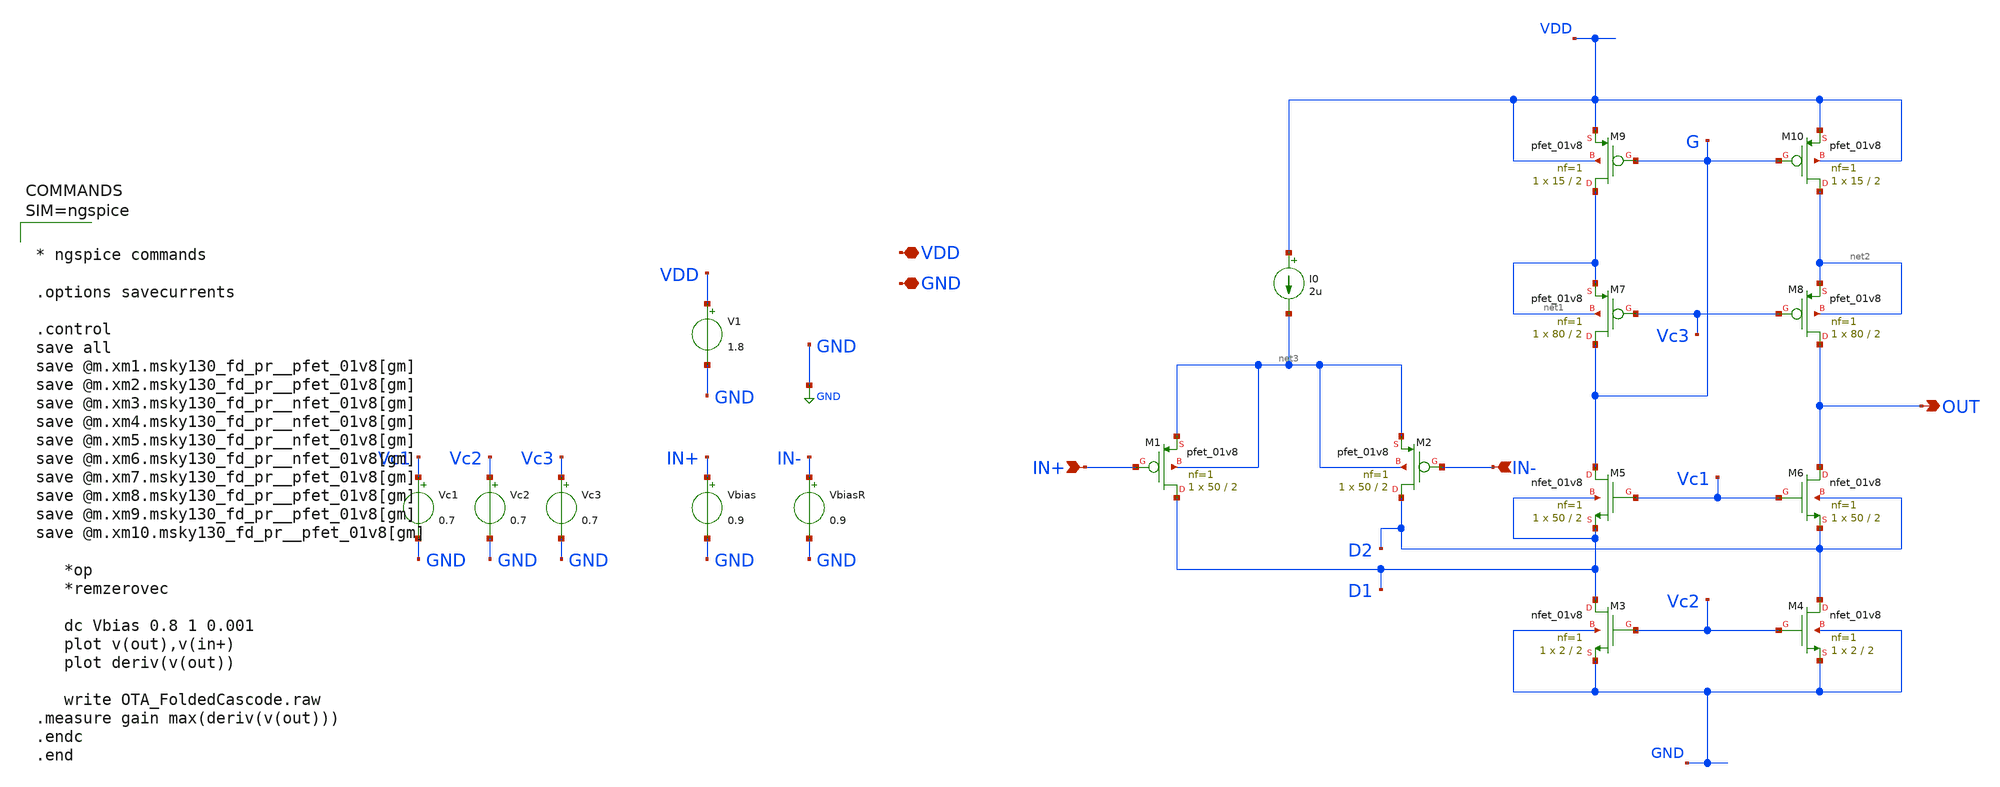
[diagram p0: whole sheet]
** sch_path: xschem/OTA_FoldedCascode.sch
**.subckt OTA_FoldedCascode VDD GND IN+ IN- OUT
*.iopin VDD
*.iopin GND
*.ipin IN+
*.ipin IN-
*.opin OUT
V1 VDD GND 1.8
Vbias IN+ GND 0.9
VbiasR IN- GND 0.9
I0 VDD net3 2u
XM1 D1 IN+ net3 net3 sky130_fd_pr__pfet_01v8 L=2 W=50 nf=1 ad='int((nf+1)/2) * W/nf * 0.29' as='int((nf+2)/2) * W/nf * 0.29'
+ pd='2*int((nf+1)/2) * (W/nf + 0.29)' ps='2*int((nf+2)/2) * (W/nf + 0.29)' nrd='0.29 / W' nrs='0.29 / W'
+ sa=0 sb=0 sd=0 mult=1 m=1
XM2 D2 IN- net3 net3 sky130_fd_pr__pfet_01v8 L=2 W=50 nf=1 ad='int((nf+1)/2) * W/nf * 0.29' as='int((nf+2)/2) * W/nf * 0.29'
+ pd='2*int((nf+1)/2) * (W/nf + 0.29)' ps='2*int((nf+2)/2) * (W/nf + 0.29)' nrd='0.29 / W' nrs='0.29 / W'
+ sa=0 sb=0 sd=0 mult=1 m=1
XM3 D1 Vc2 GND GND sky130_fd_pr__nfet_01v8 L=2 W=2 nf=1 ad='int((nf+1)/2) * W/nf * 0.29' as='int((nf+2)/2) * W/nf * 0.29'
+ pd='2*int((nf+1)/2) * (W/nf + 0.29)' ps='2*int((nf+2)/2) * (W/nf + 0.29)' nrd='0.29 / W' nrs='0.29 / W'
+ sa=0 sb=0 sd=0 mult=1 m=1
XM4 D2 Vc2 GND GND sky130_fd_pr__nfet_01v8 L=2 W=2 nf=1 ad='int((nf+1)/2) * W/nf * 0.29' as='int((nf+2)/2) * W/nf * 0.29'
+ pd='2*int((nf+1)/2) * (W/nf + 0.29)' ps='2*int((nf+2)/2) * (W/nf + 0.29)' nrd='0.29 / W' nrs='0.29 / W'
+ sa=0 sb=0 sd=0 mult=1 m=1
XM5 G Vc1 D1 D1 sky130_fd_pr__nfet_01v8 L=2 W=50 nf=1 ad='int((nf+1)/2) * W/nf * 0.29' as='int((nf+2)/2) * W/nf * 0.29'
+ pd='2*int((nf+1)/2) * (W/nf + 0.29)' ps='2*int((nf+2)/2) * (W/nf + 0.29)' nrd='0.29 / W' nrs='0.29 / W'
+ sa=0 sb=0 sd=0 mult=1 m=1
XM6 OUT Vc1 D2 D2 sky130_fd_pr__nfet_01v8 L=2 W=50 nf=1 ad='int((nf+1)/2) * W/nf * 0.29' as='int((nf+2)/2) * W/nf * 0.29'
+ pd='2*int((nf+1)/2) * (W/nf + 0.29)' ps='2*int((nf+2)/2) * (W/nf + 0.29)' nrd='0.29 / W' nrs='0.29 / W'
+ sa=0 sb=0 sd=0 mult=1 m=1
XM7 G Vc3 net1 net1 sky130_fd_pr__pfet_01v8 L=2 W=80 nf=1 ad='int((nf+1)/2) * W/nf * 0.29' as='int((nf+2)/2) * W/nf * 0.29'
+ pd='2*int((nf+1)/2) * (W/nf + 0.29)' ps='2*int((nf+2)/2) * (W/nf + 0.29)' nrd='0.29 / W' nrs='0.29 / W'
+ sa=0 sb=0 sd=0 mult=1 m=1
XM8 OUT Vc3 net2 net2 sky130_fd_pr__pfet_01v8 L=2 W=80 nf=1 ad='int((nf+1)/2) * W/nf * 0.29' as='int((nf+2)/2) * W/nf * 0.29'
+ pd='2*int((nf+1)/2) * (W/nf + 0.29)' ps='2*int((nf+2)/2) * (W/nf + 0.29)' nrd='0.29 / W' nrs='0.29 / W'
+ sa=0 sb=0 sd=0 mult=1 m=1
XM9 net1 G VDD VDD sky130_fd_pr__pfet_01v8 L=2 W=15 nf=1 ad='int((nf+1)/2) * W/nf * 0.29' as='int((nf+2)/2) * W/nf * 0.29'
+ pd='2*int((nf+1)/2) * (W/nf + 0.29)' ps='2*int((nf+2)/2) * (W/nf + 0.29)' nrd='0.29 / W' nrs='0.29 / W'
+ sa=0 sb=0 sd=0 mult=1 m=1
XM10 net2 G VDD VDD sky130_fd_pr__pfet_01v8 L=2 W=15 nf=1 ad='int((nf+1)/2) * W/nf * 0.29' as='int((nf+2)/2) * W/nf * 0.29'
+ pd='2*int((nf+1)/2) * (W/nf + 0.29)' ps='2*int((nf+2)/2) * (W/nf + 0.29)' nrd='0.29 / W' nrs='0.29 / W'
+ sa=0 sb=0 sd=0 mult=1 m=1
Vc1 Vc1 GND 0.7
Vc2 Vc2 GND 0.7
Vc3 Vc3 GND 0.7
**** begin user architecture code



* ngspice commands

.options savecurrents

.control
save all
save @m.xm1.msky130_fd_pr__pfet_01v8[gm]
save @m.xm2.msky130_fd_pr__pfet_01v8[gm]
save @m.xm3.msky130_fd_pr__nfet_01v8[gm]
save @m.xm4.msky130_fd_pr__nfet_01v8[gm]
save @m.xm5.msky130_fd_pr__nfet_01v8[gm]
save @m.xm6.msky130_fd_pr__nfet_01v8[gm]
save @m.xm7.msky130_fd_pr__pfet_01v8[gm]
save @m.xm8.msky130_fd_pr__pfet_01v8[gm]
save @m.xm9.msky130_fd_pr__pfet_01v8[gm]
save @m.xm10.msky130_fd_pr__pfet_01v8[gm]

   *op
   *remzerovec

   dc Vbias 0.8 1 0.001
   plot v(out),v(in+)
   plot deriv(v(out))

   write OTA_FoldedCascode.raw
.measure gain max(deriv(v(out)))
.endc
.end



.lib $::SKYWATER_MODELS/sky130.lib.spice tt
**** end user architecture code
**.ends
.GLOBAL GND
.end
